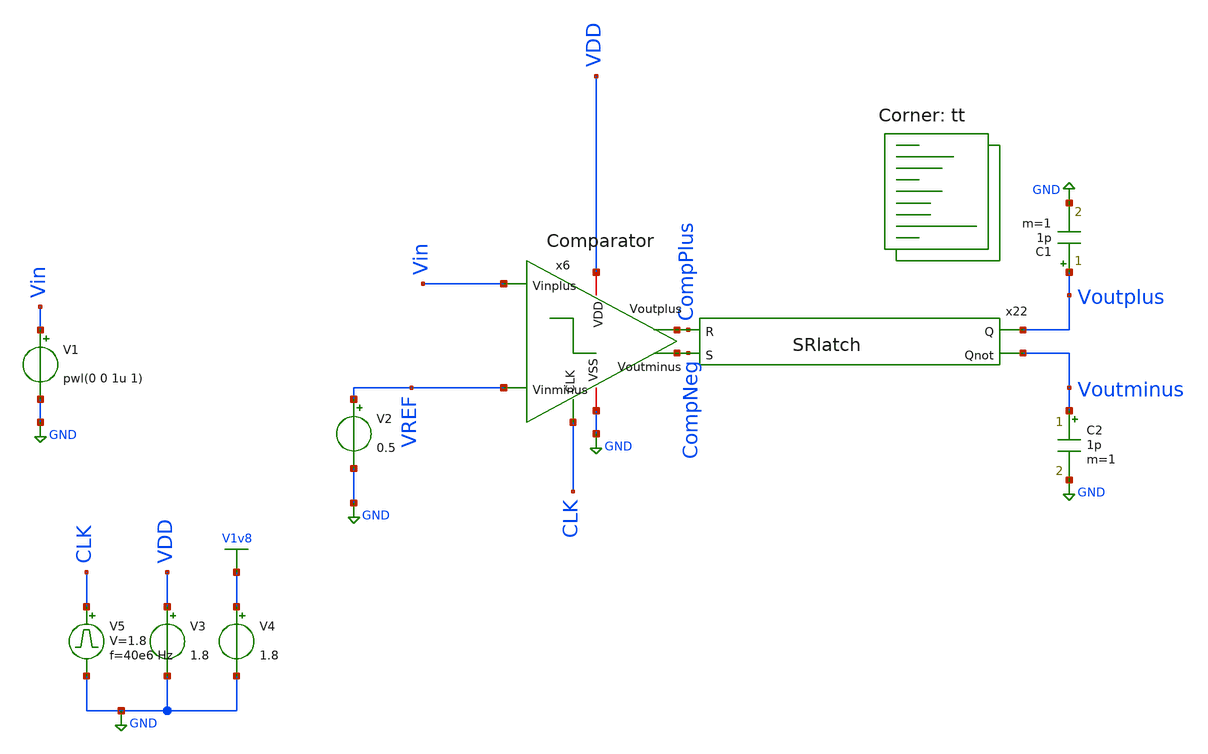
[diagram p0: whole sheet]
** sch_path: xschem/TestBenches/ComparatorTB.sch
**.subckt ComparatorTB
V2 VREF GND 0.5
V3 VDD GND 1.8
.save i(v3)
V1 Vin GND pwl(0 0 1u 1)
C1 Voutplus GND 1p m=1
C2 Voutminus GND 1p m=1
V5 CLK GND pulse 0 1.8 '0.495/ 40e6 ' '0.01/40e6 ' '0.01/40e6 ' '0.49/40e6 ' '1/40e6 '
V4 V1v8 GND 1.8
.save i(v4)
x6 VDD CompNeg CompPlus CLK Vin VREF GND Comparator
x22 Voutplus Voutminus CompPlus CompNeg SRlatch
**** begin user architecture code


.savecurrents
.control
 save all
 op
 print x1.Viominus x1.Vioplus
 print @m.x1.xm11.msky130_fd_pr__pfet_01v8_lvt[id]
 print @m.x1.xm11.msky130_fd_pr__pfet_01v8_lvt[vds] - @m.x1.xm11.msky130_fd_pr__pfet_01v8_lvt[vth]
 print @m.x1.xm23.msky130_fd_pr__pfet_01v8_lvt[vds] - @m.x1.xm23.msky130_fd_pr__pfet_01v8_lvt[vth]
 print @m.x1.xm11.msky130_fd_pr__pfet_01v8_lvt[gm]
 tran 1e-9 1u
 *dc V1 0 1.8 0.1
 plot tran.Voutplus tran.Voutminus tran.vref
 plot tran.x1.VoutplusB tran.x1.VoutminusB tran.vref
 plot Vin CLK
 plot Vin


 let Vdif = Vin - Vref
 let Voutdiff= Voutplus-Voutminus
 *plot Vdif Voutdiff
 plot i(V3)
 plot x1.Viominus x1.Vioplus
 plot dc.x1.Viominus dc.x1.Vioplus
 write ComparatorTB.raw
.endc


.lib $::SKYWATER_MODELS/sky130.lib.spice tt
Cgg = 1.021899e-14
**** end user architecture code
**.ends
.GLOBAL GND
.GLOBAL V1v8
.end
